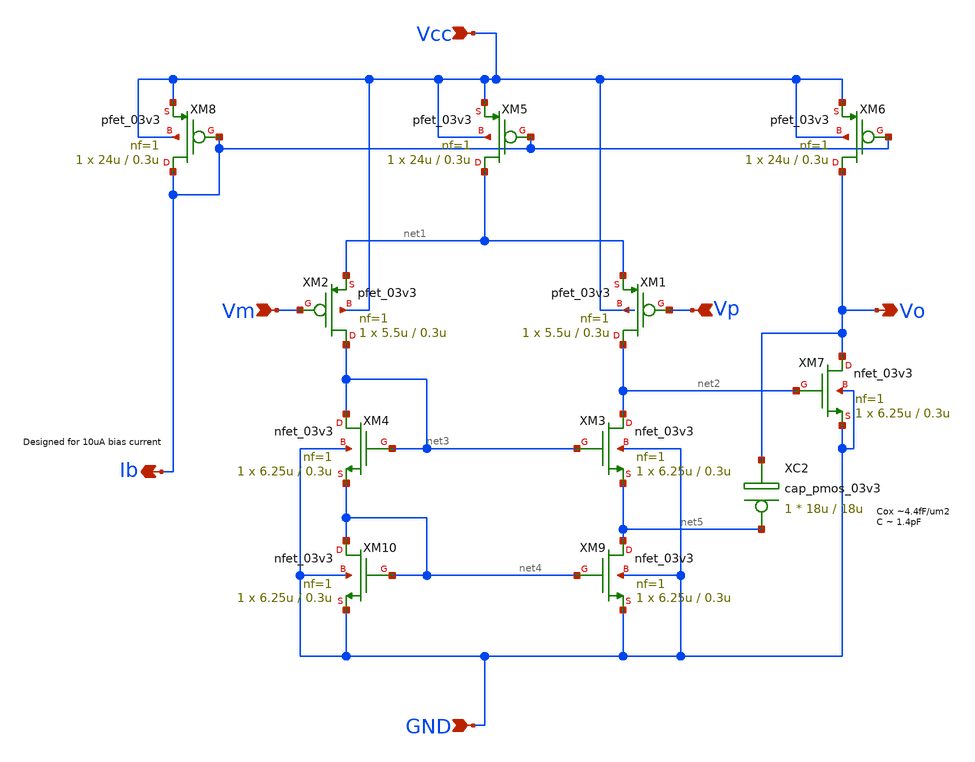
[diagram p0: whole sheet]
** sch_path: op_amp_module.sch
**.subckt op_amp_module Vm Vp Vcc GND Ib Vo
*.ipin Vm
*.ipin Vp
*.ipin Vcc
*.ipin GND
*.opin Ib
*.opin Vo
XM4 net3 net3 net4 GND nfet_03v3 L=0.3u W=6.25u nf=1 ad='int((nf+1)/2) * W/nf * 0.18u' as='int((nf+2)/2) * W/nf * 0.18u'
+ pd='2*int((nf+1)/2) * (W/nf + 0.18u)' ps='2*int((nf+2)/2) * (W/nf + 0.18u)' nrd='0.18u / W' nrs='0.18u / W'
+ sa=0 sb=0 sd=0 m=1 par=1
XM2 net3 Vm net1 Vcc pfet_03v3 L=0.3u W=5.5u nf=1 ad='int((nf+1)/2) * W/nf * 0.18u' as='int((nf+2)/2) * W/nf * 0.18u'
+ pd='2*int((nf+1)/2) * (W/nf + 0.18u)' ps='2*int((nf+2)/2) * (W/nf + 0.18u)' nrd='0.18u / W' nrs='0.18u / W'
+ sa=0 sb=0 sd=0 m=1 par=1
XM3 net2 net3 net5 GND nfet_03v3 L=0.3u W=6.25u nf=1 ad='int((nf+1)/2) * W/nf * 0.18u' as='int((nf+2)/2) * W/nf * 0.18u'
+ pd='2*int((nf+1)/2) * (W/nf + 0.18u)' ps='2*int((nf+2)/2) * (W/nf + 0.18u)' nrd='0.18u / W' nrs='0.18u / W'
+ sa=0 sb=0 sd=0 m=1 par=1
XM1 net2 Vp net1 Vcc pfet_03v3 L=0.3u W=5.5u nf=1 ad='int((nf+1)/2) * W/nf * 0.18u' as='int((nf+2)/2) * W/nf * 0.18u'
+ pd='2*int((nf+1)/2) * (W/nf + 0.18u)' ps='2*int((nf+2)/2) * (W/nf + 0.18u)' nrd='0.18u / W' nrs='0.18u / W'
+ sa=0 sb=0 sd=0 m=1 par=1
XM5 net1 Ib Vcc Vcc pfet_03v3 L=0.3u W=24u nf=1 ad='int((nf+1)/2) * W/nf * 0.18u' as='int((nf+2)/2) * W/nf * 0.18u'
+ pd='2*int((nf+1)/2) * (W/nf + 0.18u)' ps='2*int((nf+2)/2) * (W/nf + 0.18u)' nrd='0.18u / W' nrs='0.18u / W'
+ sa=0 sb=0 sd=0 m=1 par=1
XM6 Vo Ib Vcc Vcc pfet_03v3 L=0.3u W=24u nf=1 ad='int((nf+1)/2) * W/nf * 0.18u' as='int((nf+2)/2) * W/nf * 0.18u'
+ pd='2*int((nf+1)/2) * (W/nf + 0.18u)' ps='2*int((nf+2)/2) * (W/nf + 0.18u)' nrd='0.18u / W' nrs='0.18u / W'
+ sa=0 sb=0 sd=0 m=1 par=1
XM8 Ib Ib Vcc Vcc pfet_03v3 L=0.3u W=24u nf=1 ad='int((nf+1)/2) * W/nf * 0.18u' as='int((nf+2)/2) * W/nf * 0.18u'
+ pd='2*int((nf+1)/2) * (W/nf + 0.18u)' ps='2*int((nf+2)/2) * (W/nf + 0.18u)' nrd='0.18u / W' nrs='0.18u / W'
+ sa=0 sb=0 sd=0 m=1 par=1
XM7 Vo net2 GND GND nfet_03v3 L=0.3u W=6.25u nf=1 ad='int((nf+1)/2) * W/nf * 0.18u' as='int((nf+2)/2) * W/nf * 0.18u'
+ pd='2*int((nf+1)/2) * (W/nf + 0.18u)' ps='2*int((nf+2)/2) * (W/nf + 0.18u)' nrd='0.18u / W' nrs='0.18u / W'
+ sa=0 sb=0 sd=0 m=1 par=1
XM10 net4 net4 GND GND nfet_03v3 L=0.3u W=6.25u nf=1 ad='int((nf+1)/2) * W/nf * 0.18u' as='int((nf+2)/2) * W/nf * 0.18u'
+ pd='2*int((nf+1)/2) * (W/nf + 0.18u)' ps='2*int((nf+2)/2) * (W/nf + 0.18u)' nrd='0.18u / W' nrs='0.18u / W'
+ sa=0 sb=0 sd=0 m=1 par=1
XM9 net5 net4 GND GND nfet_03v3 L=0.3u W=6.25u nf=1 ad='int((nf+1)/2) * W/nf * 0.18u' as='int((nf+2)/2) * W/nf * 0.18u'
+ pd='2*int((nf+1)/2) * (W/nf + 0.18u)' ps='2*int((nf+2)/2) * (W/nf + 0.18u)' nrd='0.18u / W' nrs='0.18u / W'
+ sa=0 sb=0 sd=0 m=1 par=1
XC2 net5 Vo cap_pmos_03v3 c_width=18u c_length=18u m=1
**.ends
.end
